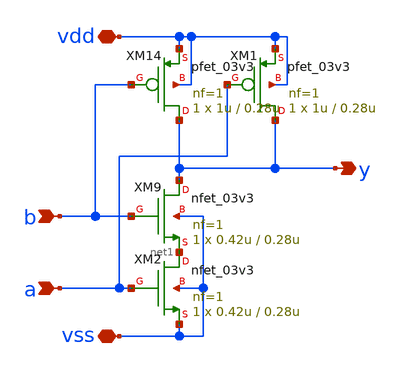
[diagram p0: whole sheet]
** sch_path: member_project/ice458/dynamic_comparator/xschem/nand.sch
**.subckt nand vdd vss a b y
*.iopin vdd
*.iopin vss
*.ipin a
*.ipin b
*.opin y
XM14 y b vdd vdd pfet_03v3 L=0.28u W=1u nf=1 ad='int((nf+1)/2) * W/nf * 0.18u' as='int((nf+2)/2) * W/nf * 0.18u'
+ pd='2*int((nf+1)/2) * (W/nf + 0.18u)' ps='2*int((nf+2)/2) * (W/nf + 0.18u)' nrd='0.18u / W' nrs='0.18u / W'
+ sa=0 sb=0 sd=0 m=1
XM9 y b net1 vss nfet_03v3 L=0.28u W=0.42u nf=1 ad='int((nf+1)/2) * W/nf * 0.18u' as='int((nf+2)/2) * W/nf * 0.18u'
+ pd='2*int((nf+1)/2) * (W/nf + 0.18u)' ps='2*int((nf+2)/2) * (W/nf + 0.18u)' nrd='0.18u / W' nrs='0.18u / W'
+ sa=0 sb=0 sd=0 m=1
XM1 y a vdd vdd pfet_03v3 L=0.28u W=1u nf=1 ad='int((nf+1)/2) * W/nf * 0.18u' as='int((nf+2)/2) * W/nf * 0.18u'
+ pd='2*int((nf+1)/2) * (W/nf + 0.18u)' ps='2*int((nf+2)/2) * (W/nf + 0.18u)' nrd='0.18u / W' nrs='0.18u / W'
+ sa=0 sb=0 sd=0 m=1
XM2 net1 a vss vss nfet_03v3 L=0.28u W=0.42u nf=1 ad='int((nf+1)/2) * W/nf * 0.18u' as='int((nf+2)/2) * W/nf * 0.18u'
+ pd='2*int((nf+1)/2) * (W/nf + 0.18u)' ps='2*int((nf+2)/2) * (W/nf + 0.18u)' nrd='0.18u / W' nrs='0.18u / W'
+ sa=0 sb=0 sd=0 m=1
**.ends
.end
